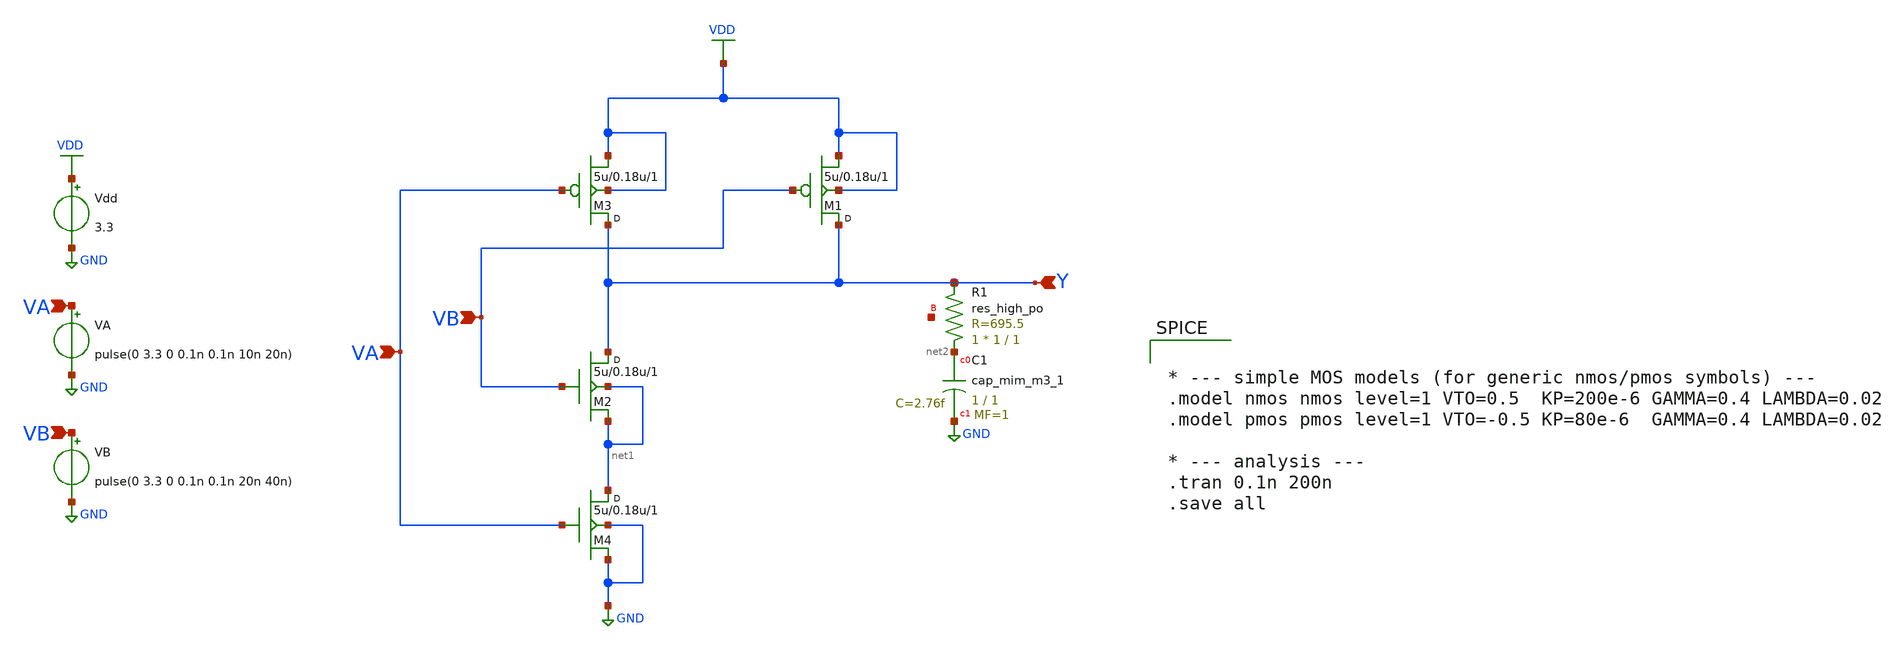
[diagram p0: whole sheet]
** sch_path: units/top/ana/cells/nand/nand.sch
**.subckt nand Y VA VA VB VB
*.ipin Y
*.ipin VA
*.ipin VA
*.ipin VB
*.ipin VB
M2 Y VB net1 net1 nmos w=5u l=0.18u m=1
M3 Y VA VDD VDD pmos w=5u l=0.18u m=1
Vdd VDD GND 3.3
.save i(vdd)
M1 Y VB VDD VDD pmos w=5u l=0.18u m=1
M4 net1 VA GND GND nmos w=5u l=0.18u m=1
XR1 net2 Y net3 sky130_fd_pr__res_high_po W=1 L=1 mult=1 m=1
XC1 net2 GND sky130_fd_pr__cap_mim_m3_1 W=1 L=1 MF=1 m=1
VA VA GND pulse(0 3.3 0 0.1n 0.1n 10n 20n)
VB VB GND pulse(0 3.3 0 0.1n 0.1n 20n 40n)
**** begin user architecture code


.lib /usr/local/share/pdk/sky130B/libs.tech/ngspice/sky130.lib.spice tt
.option wnflag=1

.save v(VA) v(VB) v(Y)

.option rawfmt=psfascii
.control
run
wrdata nand.raw v(VA) v(VB) v(Y)
.endc






* --- simple MOS models (for generic nmos/pmos symbols) ---
.model nmos nmos level=1 VTO=0.5  KP=200e-6 GAMMA=0.4 LAMBDA=0.02
.model pmos pmos level=1 VTO=-0.5 KP=80e-6  GAMMA=0.4 LAMBDA=0.02

* --- analysis ---
.tran 0.1n 200n
.save all


**** end user architecture code
**.ends
.GLOBAL VDD
.GLOBAL GND
.end
